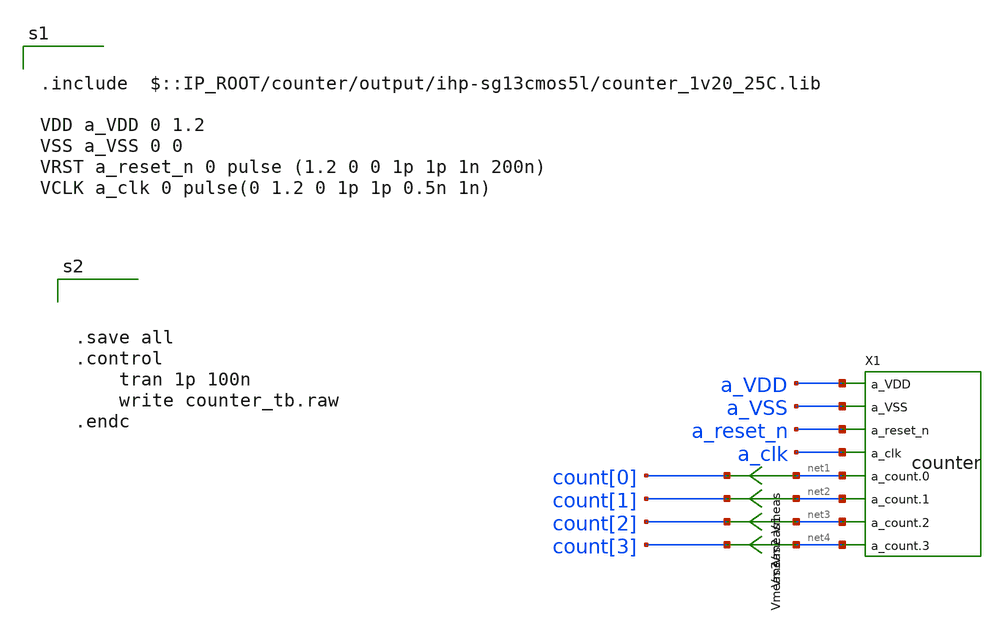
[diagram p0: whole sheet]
** sch_path: counter/counter_tb.sch
**.subckt counter_tb
X1 a_VDD a_VSS a_reset_n a_clk net1 net2 net3 net4 counter
Vmeas net1 count[0] 0
.save i(vmeas)
Vmeas1 net2 count[1] 0
.save i(vmeas1)
Vmeas2 net3 count[2] 0
.save i(vmeas2)
Vmeas3 net4 count[3] 0
.save i(vmeas3)
**** begin user architecture code

.include  $::IP_ROOT/counter/output/ihp-sg13cmos5l/counter_1v20_25C.lib

VDD a_VDD 0 1.2
VSS a_VSS 0 0
VRST a_reset_n 0 pulse (1.2 0 0 1p 1p 1n 200n)
VCLK a_clk 0 pulse(0 1.2 0 1p 1p 0.5n 1n)





.save all
.control
	tran 1p 100n
	write counter_tb.raw
.endc



**** end user architecture code
**.ends
.end
